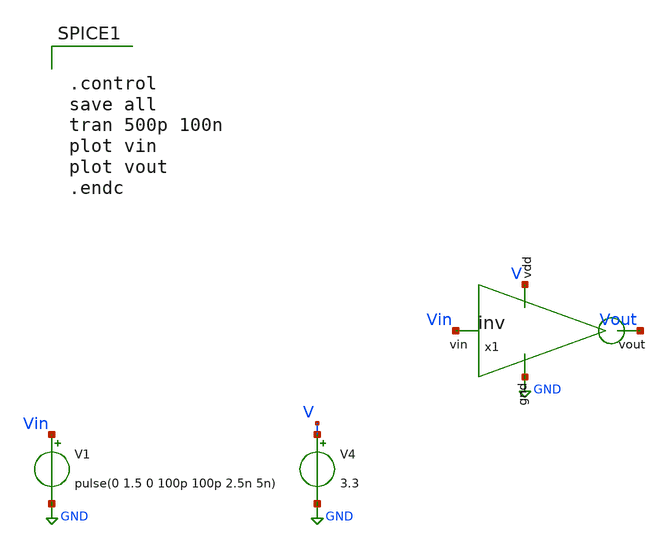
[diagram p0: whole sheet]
** sch_path: comparator/testbench/inverter__tb.sch
**.subckt inverter__tb
V1 Vin GND pulse(0 1.5 0 100p 100p 2.5n 5n)
V4 V GND 3.3
x1 V GND Vout Vin inv cl=0.28u wp=0.44u wn=0.22u
**** begin user architecture code


.control
save all
tran 500p 100n
plot vin
plot vout
.endc


.include /foss/pdks/gf180mcuC/libs.tech/ngspice/design.ngspice
.lib /foss/pdks/gf180mcuC/libs.tech/ngspice/sm141064.ngspice typical

**** end user architecture code
**.ends

* expanding   symbol:  symbols/inv.sym # of pins=4
** sym_path: symbols/inv.sym
** sch_path: symbols/inv.sch
.subckt inv vdd gnd vout vin  cl=0.28u wp=0.44u wn=0.22u
*.ipin gnd
*.ipin vdd
*.ipin vin
*.opin vout
XM1 gnd vin vout gnd nfet_03v3 L=0.28u W=.22u nf=1 ad='int((nf+1)/2) * W/nf * 0.18u' as='int((nf+2)/2) * W/nf * 0.18u'
+ pd='2*int((nf+1)/2) * (W/nf + 0.18u)' ps='2*int((nf+2)/2) * (W/nf + 0.18u)' nrd='0.18u / W' nrs='0.18u / W'
+ sa=0 sb=0 sd=0 m=1
XM2 vdd vin vout vdd pfet_03v3 L=0.28u W=.22u nf=1 ad='int((nf+1)/2) * W/nf * 0.18u' as='int((nf+2)/2) * W/nf * 0.18u'
+ pd='2*int((nf+1)/2) * (W/nf + 0.18u)' ps='2*int((nf+2)/2) * (W/nf + 0.18u)' nrd='0.18u / W' nrs='0.18u / W'
+ sa=0 sb=0 sd=0 m=1
.ends

.GLOBAL GND
.end
